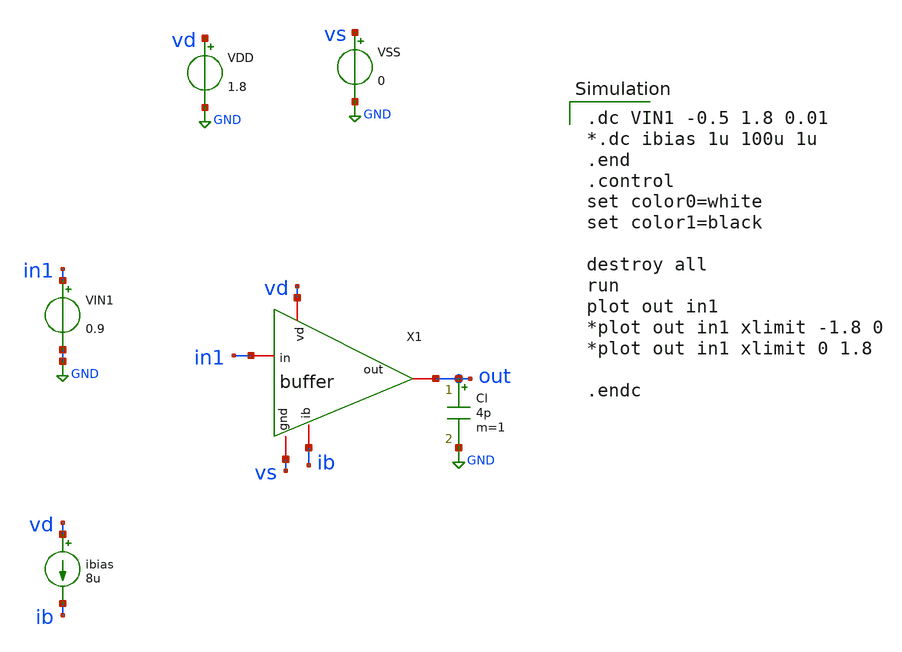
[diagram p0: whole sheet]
** sch_path: buffer/xschem/buffer_tb-dc.sch
* Copyright 2020 Stefan Frederik Schippers
* Licensed under the Apache License, Version 2.0 (the "License");
* you may not use this file except in compliance with the License.
* You may obtain a copy of the License at
* https://www.apache.org/licenses/LICENSE-2.0
* Unless required by applicable law or agreed to in writing, software
* distributed under the License is distributed on an "AS IS" BASIS,
* WITHOUT WARRANTIES OR CONDITIONS OF ANY KIND, either express or implied.
* See the License for the specific language governing permissions and
* limitations under the License.
**.subckt buffer_tb-dc
VIN1 in1 GND 0.9
ibias vd ib 8u
VDD vd GND 1.8
VSS vs GND 0
X1 vd in1 out ib vs buffer
Cl out GND 4p m=1
**** begin user architecture code

.dc VIN1 -0.5 1.8 0.01
*.dc ibias 1u 100u 1u
.end
.control
set color0=white
set color1=black

destroy all
run
plot out in1
*plot out in1 xlimit -1.8 0
*plot out in1 xlimit 0 1.8

.endc

 .lib $::SKYWATER_MODELS/sky130.lib.spice tt
.include $::SKYWATER_STDCELLS/sky130_fd_sc_hd.spice

**** end user architecture code
**.ends

* expanding   symbol:  /home/hugodg/projects-sky130/temp-sensor/buffer/xschem/buffer.sym # of pins=5
** sym_path: buffer/xschem/buffer.sym
** sch_path: buffer/xschem/buffer.sch
.subckt buffer vd in out ib gnd
*.iopin vd
*.iopin ib
*.iopin out
*.iopin in
*.iopin gnd
**** begin user architecture code




**** end user architecture code
XM3 net2 net2 vd vd sky130_fd_pr__pfet_01v8 L=1 W=1 nf=1 ad='int((nf+1)/2) * W/nf * 0.29' as='int((nf+2)/2) * W/nf * 0.29'
+ pd='2*int((nf+1)/2) * (W/nf + 0.29)' ps='2*int((nf+2)/2) * (W/nf + 0.29)' nrd='0.29 / W' nrs='0.29 / W'
+ sa=0 sb=0 sd=0 mult=1 m=1
XM1 net2 out net3 net3 sky130_fd_pr__nfet_01v8 L=1 W=10 nf=1 ad='int((nf+1)/2) * W/nf * 0.29' as='int((nf+2)/2) * W/nf * 0.29'
+ pd='2*int((nf+1)/2) * (W/nf + 0.29)' ps='2*int((nf+2)/2) * (W/nf + 0.29)' nrd='0.29 / W' nrs='0.29 / W'
+ sa=0 sb=0 sd=0 mult=1 m=1
XM2 net4 in net3 net3 sky130_fd_pr__nfet_01v8 L=1 W=10 nf=1 ad='int((nf+1)/2) * W/nf * 0.29' as='int((nf+2)/2) * W/nf * 0.29'
+ pd='2*int((nf+1)/2) * (W/nf + 0.29)' ps='2*int((nf+2)/2) * (W/nf + 0.29)' nrd='0.29 / W' nrs='0.29 / W'
+ sa=0 sb=0 sd=0 mult=1 m=1
XM4 net4 net4 vd vd sky130_fd_pr__pfet_01v8 L=1 W=1 nf=1 ad='int((nf+1)/2) * W/nf * 0.29' as='int((nf+2)/2) * W/nf * 0.29'
+ pd='2*int((nf+1)/2) * (W/nf + 0.29)' ps='2*int((nf+2)/2) * (W/nf + 0.29)' nrd='0.29 / W' nrs='0.29 / W'
+ sa=0 sb=0 sd=0 mult=1 m=1
XM5 net3 ib gnd gnd sky130_fd_pr__nfet_01v8 L=1 W=1 nf=1 ad='int((nf+1)/2) * W/nf * 0.29' as='int((nf+2)/2) * W/nf * 0.29'
+ pd='2*int((nf+1)/2) * (W/nf + 0.29)' ps='2*int((nf+2)/2) * (W/nf + 0.29)' nrd='0.29 / W' nrs='0.29 / W'
+ sa=0 sb=0 sd=0 mult=1 m=1
XM6 out net4 vd vd sky130_fd_pr__pfet_01v8 L=1 W=10 nf=1 ad='int((nf+1)/2) * W/nf * 0.29' as='int((nf+2)/2) * W/nf * 0.29'
+ pd='2*int((nf+1)/2) * (W/nf + 0.29)' ps='2*int((nf+2)/2) * (W/nf + 0.29)' nrd='0.29 / W' nrs='0.29 / W'
+ sa=0 sb=0 sd=0 mult=1 m=1
XM7 out net1 gnd gnd sky130_fd_pr__nfet_01v8 L=1 W=10 nf=1 ad='int((nf+1)/2) * W/nf * 0.29' as='int((nf+2)/2) * W/nf * 0.29'
+ pd='2*int((nf+1)/2) * (W/nf + 0.29)' ps='2*int((nf+2)/2) * (W/nf + 0.29)' nrd='0.29 / W' nrs='0.29 / W'
+ sa=0 sb=0 sd=0 mult=1 m=1
XM8 net1 net2 vd vd sky130_fd_pr__pfet_01v8 L=1 W=10 nf=1 ad='int((nf+1)/2) * W/nf * 0.29' as='int((nf+2)/2) * W/nf * 0.29'
+ pd='2*int((nf+1)/2) * (W/nf + 0.29)' ps='2*int((nf+2)/2) * (W/nf + 0.29)' nrd='0.29 / W' nrs='0.29 / W'
+ sa=0 sb=0 sd=0 mult=1 m=1
XM9 net1 net1 gnd gnd sky130_fd_pr__nfet_01v8 L=1 W=10 nf=1 ad='int((nf+1)/2) * W/nf * 0.29' as='int((nf+2)/2) * W/nf * 0.29'
+ pd='2*int((nf+1)/2) * (W/nf + 0.29)' ps='2*int((nf+2)/2) * (W/nf + 0.29)' nrd='0.29 / W' nrs='0.29 / W'
+ sa=0 sb=0 sd=0 mult=1 m=1
XM10 ib ib gnd gnd sky130_fd_pr__nfet_01v8 L=1 W=1 nf=1 ad='int((nf+1)/2) * W/nf * 0.29' as='int((nf+2)/2) * W/nf * 0.29'
+ pd='2*int((nf+1)/2) * (W/nf + 0.29)' ps='2*int((nf+2)/2) * (W/nf + 0.29)' nrd='0.29 / W' nrs='0.29 / W'
+ sa=0 sb=0 sd=0 mult=1 m=1
.ends

.GLOBAL GND
.end
